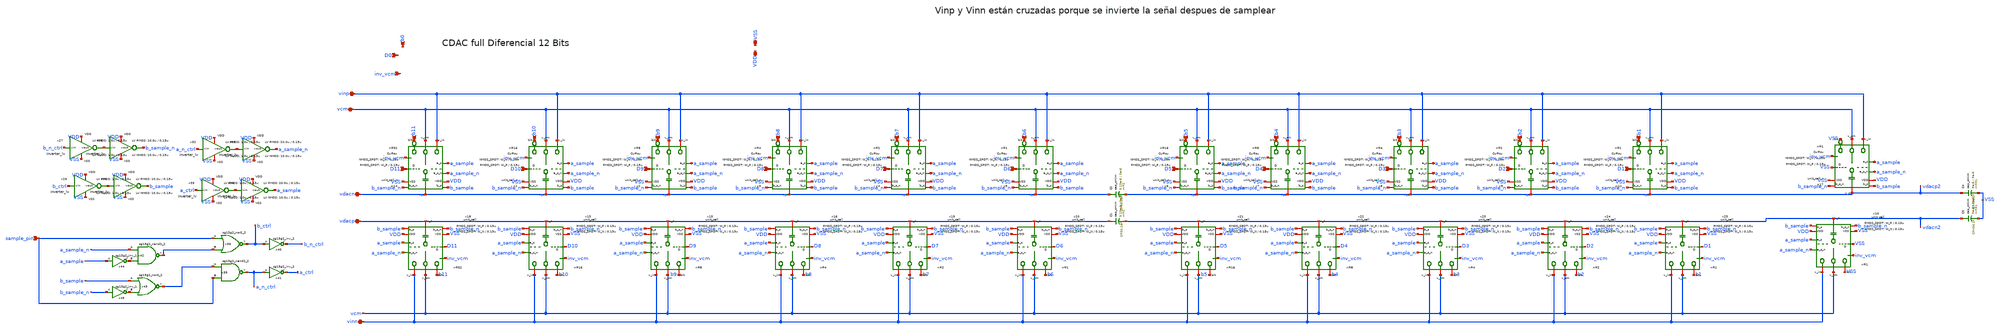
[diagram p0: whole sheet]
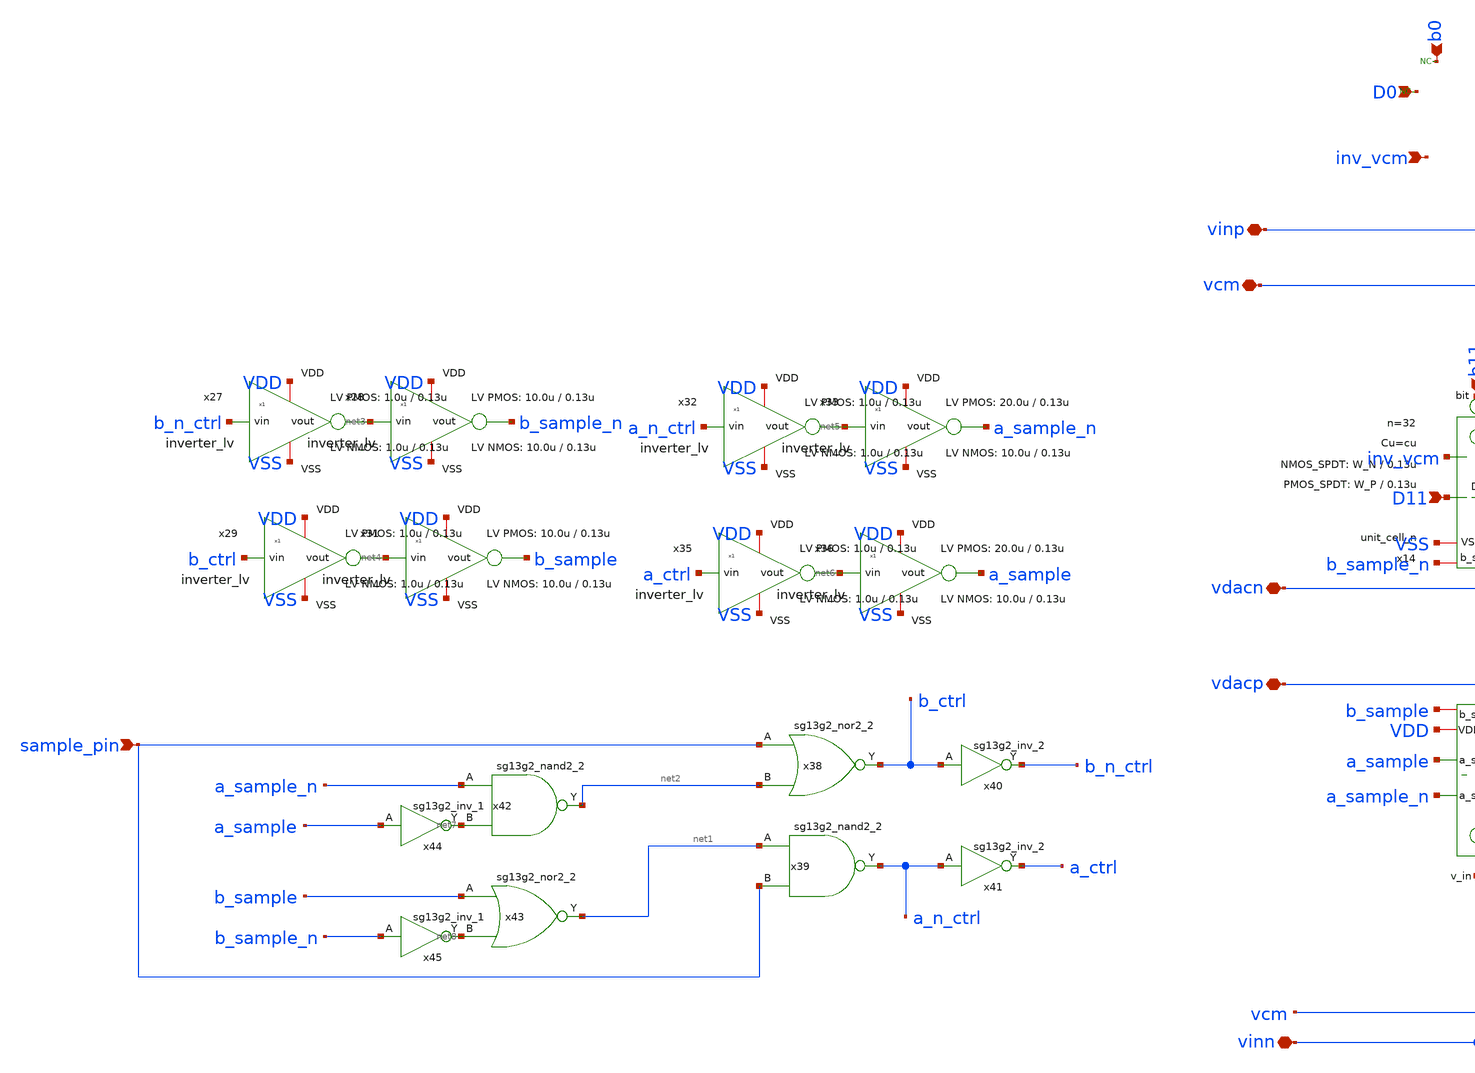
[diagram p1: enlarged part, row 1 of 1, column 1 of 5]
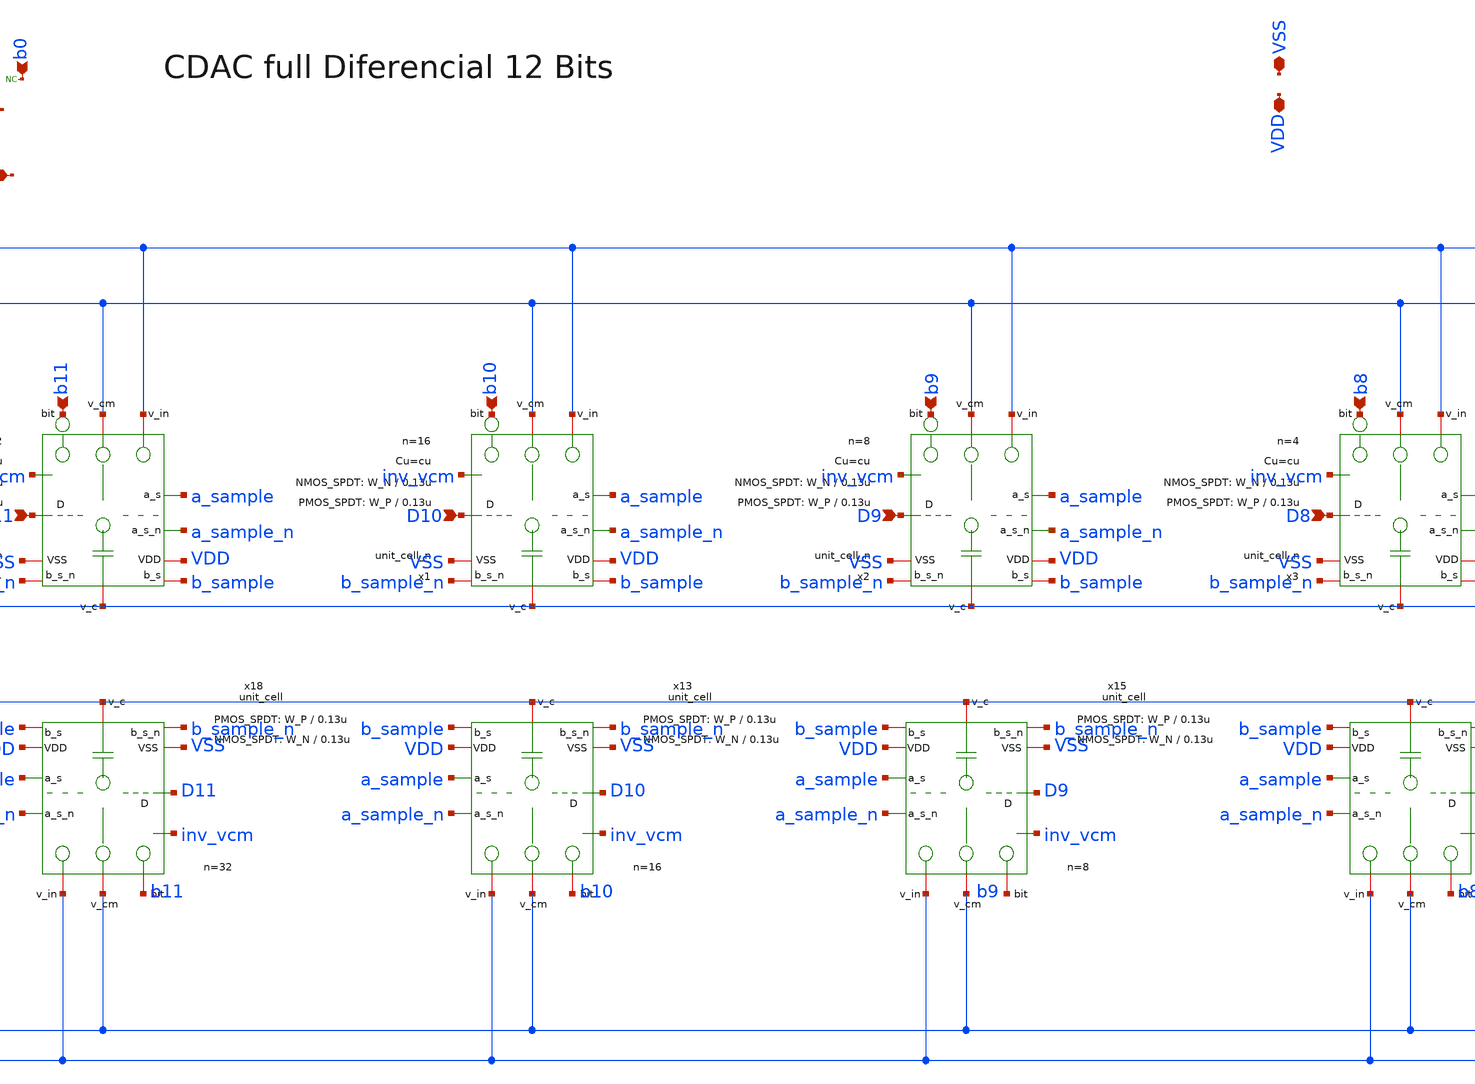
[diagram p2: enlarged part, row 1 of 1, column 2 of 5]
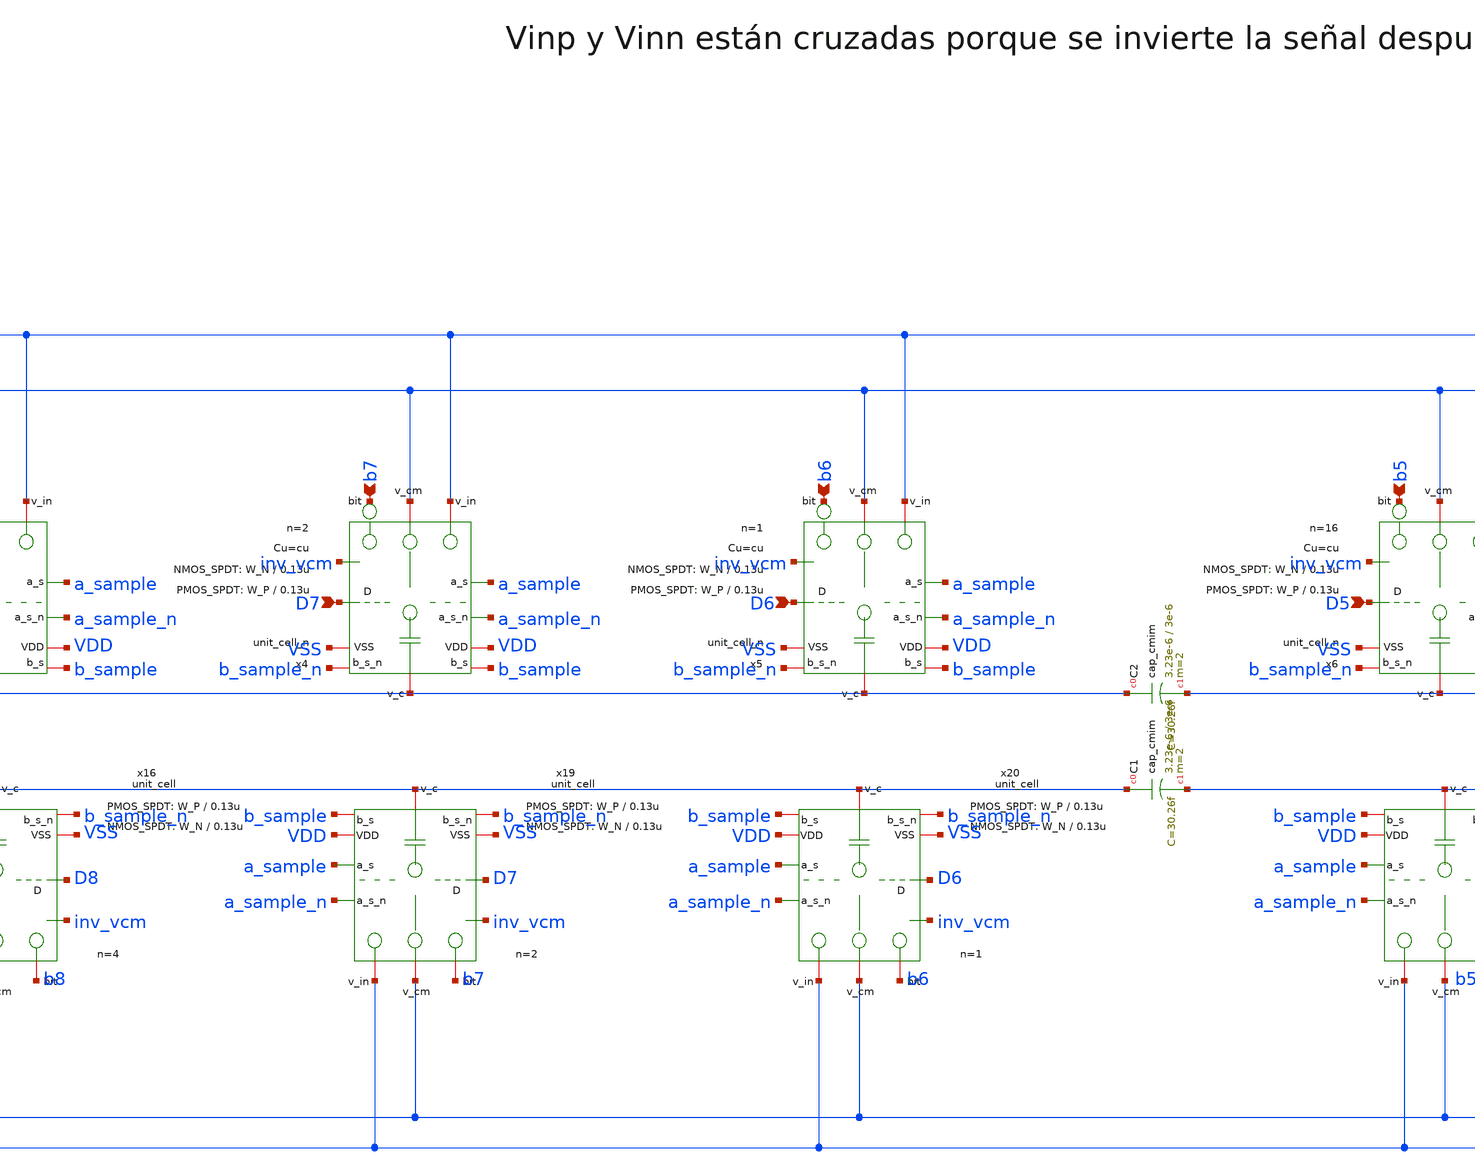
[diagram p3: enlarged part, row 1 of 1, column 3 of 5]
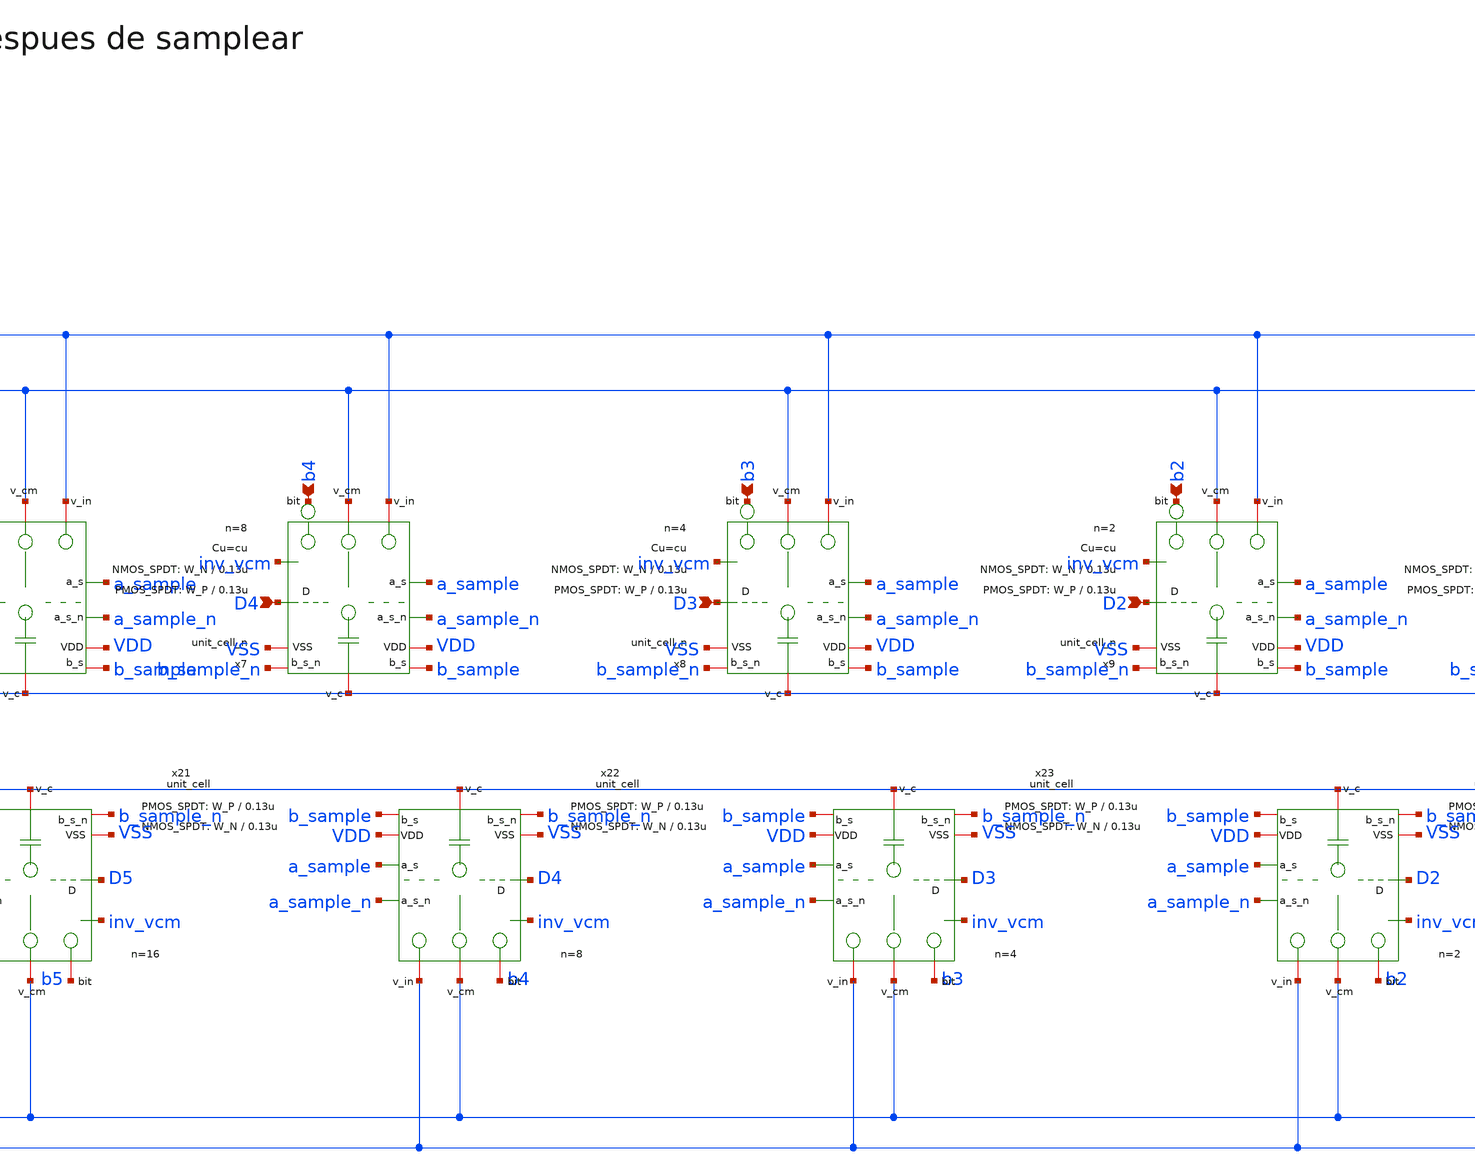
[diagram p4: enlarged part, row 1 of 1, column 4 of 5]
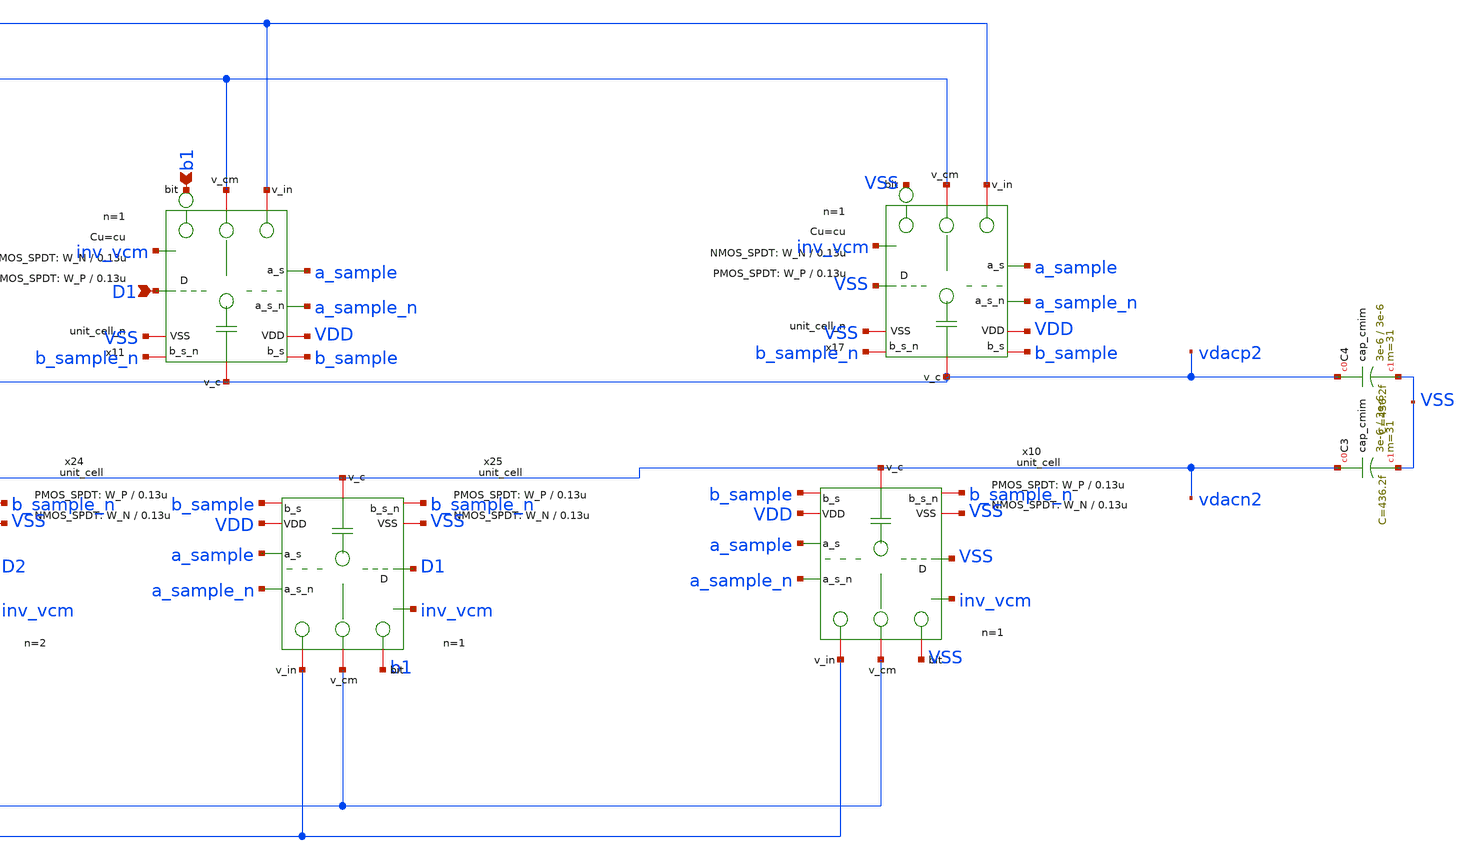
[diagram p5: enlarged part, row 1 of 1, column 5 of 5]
** sch_path: xschem/dac_icms_cell/dac.sch
* IHP-GmbH/IHP-Open-PDK/ihp-sg13g2/libs.tech/xschem/sg13g2_stdcells/sg13g2_inv_2.sch:
* Copyright 2023 IHP PDK Authors
* Licensed under the Apache License, Version 2.0 (the "License");
**.subckt dac D0 b0 vinn vcm sample_pin vinp vdacp vdacn VSS VDD D1 b1 D2 b2 D3 b3 D4 b4 D5 b5 b6 D7
*+ b7 D8 b8 D9 b9 D10 b10 D11 b11 D6 inv_vcm
*.ipin D0
*.ipin b0
*.iopin vinn
*.iopin vcm
*.ipin sample_pin
*.iopin vinp
*.iopin vdacp
*.iopin vdacn
*.iopin VSS
*.iopin VDD
*.ipin D1
*.ipin b1
*.ipin D2
*.ipin b2
*.ipin D3
*.ipin b3
*.ipin D4
*.ipin b4
*.ipin D5
*.ipin b5
*.ipin b6
*.ipin D7
*.ipin b7
*.ipin D8
*.ipin b8
*.ipin D9
*.ipin b9
*.ipin D10
*.ipin b10
*.ipin D11
*.ipin b11
*.ipin D6
*.ipin inv_vcm
x14 VDD D11 VSS vdacn b11 vcm vinp a_sample a_sample_n b_sample b_sample_n inv_vcm unit_cell_n
+ W_P_SPDT=W_P L_P_SPDT=0.13u W_N_SPDT=W_N L_N_SPDT=0.13u Cu=cu n=32
x18 VDD D11 VSS vdacp b11 vcm vinn a_sample a_sample_n b_sample b_sample_n inv_vcm unit_cell
+ W_P_SPDT=W_P L_P_SPDT=0.13u W_N_SPDT=W_N L_N_SPDT=0.13u Cu=cu n=32
x1 VDD D10 VSS vdacn b10 vcm vinp a_sample a_sample_n b_sample b_sample_n inv_vcm unit_cell_n
+ W_P_SPDT=W_P L_P_SPDT=0.13u W_N_SPDT=W_N L_N_SPDT=0.13u Cu=cu n=16
x2 VDD D9 VSS vdacn b9 vcm vinp a_sample a_sample_n b_sample b_sample_n inv_vcm unit_cell_n
+ W_P_SPDT=W_P L_P_SPDT=0.13u W_N_SPDT=W_N L_N_SPDT=0.13u Cu=cu n=8
x3 VDD D8 VSS vdacn b8 vcm vinp a_sample a_sample_n b_sample b_sample_n inv_vcm unit_cell_n
+ W_P_SPDT=W_P L_P_SPDT=0.13u W_N_SPDT=W_N L_N_SPDT=0.13u Cu=cu n=4
x4 VDD D7 VSS vdacn b7 vcm vinp a_sample a_sample_n b_sample b_sample_n inv_vcm unit_cell_n
+ W_P_SPDT=W_P L_P_SPDT=0.13u W_N_SPDT=W_N L_N_SPDT=0.13u Cu=cu n=2
x5 VDD D6 VSS vdacn b6 vcm vinp a_sample a_sample_n b_sample b_sample_n inv_vcm unit_cell_n
+ W_P_SPDT=W_P L_P_SPDT=0.13u W_N_SPDT=W_N L_N_SPDT=0.13u Cu=cu n=1
x6 VDD D5 VSS vdacp2 b5 vcm vinp a_sample a_sample_n b_sample b_sample_n inv_vcm unit_cell_n
+ W_P_SPDT=W_P L_P_SPDT=0.13u W_N_SPDT=W_N L_N_SPDT=0.13u Cu=cu n=16
x7 VDD D4 VSS vdacp2 b4 vcm vinp a_sample a_sample_n b_sample b_sample_n inv_vcm unit_cell_n
+ W_P_SPDT=W_P L_P_SPDT=0.13u W_N_SPDT=W_N L_N_SPDT=0.13u Cu=cu n=8
x8 VDD D3 VSS vdacp2 b3 vcm vinp a_sample a_sample_n b_sample b_sample_n inv_vcm unit_cell_n
+ W_P_SPDT=W_P L_P_SPDT=0.13u W_N_SPDT=W_N L_N_SPDT=0.13u Cu=cu n=4
x9 VDD D2 VSS vdacp2 b2 vcm vinp a_sample a_sample_n b_sample b_sample_n inv_vcm unit_cell_n
+ W_P_SPDT=W_P L_P_SPDT=0.13u W_N_SPDT=W_N L_N_SPDT=0.13u Cu=cu n=2
x11 VDD D1 VSS vdacp2 b1 vcm vinp a_sample a_sample_n b_sample b_sample_n inv_vcm unit_cell_n
+ W_P_SPDT=W_P L_P_SPDT=0.13u W_N_SPDT=W_N L_N_SPDT=0.13u Cu=cu n=1
x13 VDD D10 VSS vdacp b10 vcm vinn a_sample a_sample_n b_sample b_sample_n inv_vcm unit_cell
+ W_P_SPDT=W_P L_P_SPDT=0.13u W_N_SPDT=W_N L_N_SPDT=0.13u Cu=cu n=16
x15 VDD D9 VSS vdacp b9 vcm vinn a_sample a_sample_n b_sample b_sample_n inv_vcm unit_cell
+ W_P_SPDT=W_P L_P_SPDT=0.13u W_N_SPDT=W_N L_N_SPDT=0.13u Cu=cu n=8
x16 VDD D8 VSS vdacp b8 vcm vinn a_sample a_sample_n b_sample b_sample_n inv_vcm unit_cell
+ W_P_SPDT=W_P L_P_SPDT=0.13u W_N_SPDT=W_N L_N_SPDT=0.13u Cu=cu n=4
x19 VDD D7 VSS vdacp b7 vcm vinn a_sample a_sample_n b_sample b_sample_n inv_vcm unit_cell
+ W_P_SPDT=W_P L_P_SPDT=0.13u W_N_SPDT=W_N L_N_SPDT=0.13u Cu=cu n=2
x20 VDD D6 VSS vdacp b6 vcm vinn a_sample a_sample_n b_sample b_sample_n inv_vcm unit_cell
+ W_P_SPDT=W_P L_P_SPDT=0.13u W_N_SPDT=W_N L_N_SPDT=0.13u Cu=cu n=1
x21 VDD D5 VSS vdacn2 b5 vcm vinn a_sample a_sample_n b_sample b_sample_n inv_vcm unit_cell
+ W_P_SPDT=W_P L_P_SPDT=0.13u W_N_SPDT=W_N L_N_SPDT=0.13u Cu=cu n=16
x22 VDD D4 VSS vdacn2 b4 vcm vinn a_sample a_sample_n b_sample b_sample_n inv_vcm unit_cell
+ W_P_SPDT=W_P L_P_SPDT=0.13u W_N_SPDT=W_N L_N_SPDT=0.13u Cu=cu n=8
x23 VDD D3 VSS vdacn2 b3 vcm vinn a_sample a_sample_n b_sample b_sample_n inv_vcm unit_cell
+ W_P_SPDT=W_P L_P_SPDT=0.13u W_N_SPDT=W_N L_N_SPDT=0.13u Cu=cu n=4
x24 VDD D2 VSS vdacn2 b2 vcm vinn a_sample a_sample_n b_sample b_sample_n inv_vcm unit_cell
+ W_P_SPDT=W_P L_P_SPDT=0.13u W_N_SPDT=W_N L_N_SPDT=0.13u Cu=cu n=2
x25 VDD D1 VSS vdacn2 b1 vcm vinn a_sample a_sample_n b_sample b_sample_n inv_vcm unit_cell
+ W_P_SPDT=W_P L_P_SPDT=0.13u W_N_SPDT=W_N L_N_SPDT=0.13u Cu=cu n=1
x27 VDD b_n_ctrl net3 VSS inverter_lv W_P=1.0u L_P=0.13u W_N=1.0u L_N=0.13u N_C=1
x28 VDD net3 b_sample_n VSS inverter_lv W_P=10.0u L_P=0.13u W_N=10.0u L_N=0.13u N_C=1
x29 VDD b_ctrl net4 VSS inverter_lv W_P=1.0u L_P=0.13u W_N=1.0u L_N=0.13u N_C=1
x31 VDD net4 b_sample VSS inverter_lv W_P=10.0u L_P=0.13u W_N=10.0u L_N=0.13u N_C=1
x32 VDD a_n_ctrl net5 VSS inverter_lv W_P=1.0u L_P=0.13u W_N=1.0u L_N=0.13u N_C=1
x33 VDD net5 a_sample_n VSS inverter_lv W_P=20.0u L_P=0.13u W_N=10.0u L_N=0.13u N_C=1
x35 VDD a_ctrl net6 VSS inverter_lv W_P=1.0u L_P=0.13u W_N=1.0u L_N=0.13u N_C=1
x36 VDD net6 a_sample VSS inverter_lv W_P=20.0u L_P=0.13u W_N=10.0u L_N=0.13u N_C=1
x38 b_ctrl sample_pin net2 VDD VSS sg13g2_nor2_2
x39 a_n_ctrl net1 sample_pin VDD VSS sg13g2_nand2_2
x40 b_n_ctrl b_ctrl VDD VSS sg13g2_inv_2
x41 a_ctrl a_n_ctrl VDD VSS sg13g2_inv_2
x42 net2 a_sample_n net7 VDD VSS sg13g2_nand2_2
x43 net1 b_sample net8 VDD VSS sg13g2_nor2_2
x44 net7 a_sample VDD VSS sg13g2_inv_1
x45 net8 b_sample_n VDD VSS sg13g2_inv_1
XC1 vdacp vdacn2 cap_cmim w=3.23e-6 l=3e-6 m=2 mm_ok=1
XC2 vdacn vdacp2 cap_cmim w=3.23e-6 l=3e-6 m=2 mm_ok=1
x10 VDD VSS VSS vdacn2 VSS vcm vinn a_sample a_sample_n b_sample b_sample_n inv_vcm unit_cell
+ W_P_SPDT=W_P L_P_SPDT=0.13u W_N_SPDT=W_N L_N_SPDT=0.13u Cu=cu n=1
x17 VDD VSS VSS vdacp2 VSS vcm vinp a_sample a_sample_n b_sample b_sample_n inv_vcm unit_cell_n
+ W_P_SPDT=W_P L_P_SPDT=0.13u W_N_SPDT=W_N L_N_SPDT=0.13u Cu=cu n=1
XC3 vdacn2 VSS cap_cmim w=3e-6 l=3e-6 m=31 mm_ok=1
XC4 vdacp2 VSS cap_cmim w=3e-6 l=3e-6 m=31 mm_ok=1
* noconn b0
* noconn D0
**.ends

* expanding   symbol:  dac_icms_cell/unit_cell_n.sym # of pins=12
** sym_path: xschem/dac_icms_cell/unit_cell_n.sym
** sch_path: xschem/dac_icms_cell/unit_cell_n.sch
.subckt unit_cell_n VDD d VSS v_top bit v_cm v_in a_sample a_sample_n b_sample b_sample_n inv_vcm
+  W_P_SPDT=1.0u L_P_SPDT=0.13u W_N_SPDT=1.0u L_N_SPDT=0.13u Cu=8f n=1
*.iopin v_top
*.ipin a_sample
*.ipin a_sample_n
*.ipin b_sample
*.ipin b_sample_n
*.iopin v_in
*.ipin d
*.iopin v_cm
*.ipin bit
*.ipin inv_vcm
*.iopin VSS
*.iopin VDD
x2 VDD a_sample VSS v_top v_cm a_sample_n transmission_gate_lv_wo_dummy W_P=W_P_SPDT L_P=L_P_SPDT
+ W_N=W_N_SPDT L_N=L_N_SPDT W_P_D=1.0u L_P_D=0.13u W_N_D=1.0u L_N_D=0.13u n=n
XC1 TOP_C v_top cap_cmim w=3e-6 l=3e-6 m=n mm_ok=1
XM1 TOP_C net3 VSS VSS sg13_lv_nmos w=4u l=0.13u ng=1 m=n mm_ok=1
XM3 TOP_C net4 VDD VDD sg13_lv_pmos w=4u l=0.13u ng=1 m=n mm_ok=1
x3 VDD net2 VSS TOP_C v_cm net1 transmission_gate_lv_wo_dummy W_P=W_P_SPDT L_P=L_P_SPDT W_N=W_N_SPDT
+ L_N=L_N_SPDT W_P_D=1.0u L_P_D=0.13u W_N_D=1.0u L_N_D=0.13u n=n
x4 VDD b_sample_n VSS TOP_C v_in b_sample transmission_gate_lv_w_dummy W_P=W_P_SPDT L_P=L_P_SPDT
+ W_N=W_N_SPDT L_N=L_N_SPDT W_P_D=1.0u L_P_D=0.13u W_N_D=1.0u L_N_D=0.13u n=n
x23 net5 bit d VDD VSS sg13g2_nand2_1
x46 net6 net8 d VDD VSS sg13g2_and2_1
x5 VDD net5 net4 VSS buffer_lv W_P_INV=3.0u L_P_INV=0.13u W_N_INV=1.0u L_N_INV=0.13u
x6 VDD net6 net3 VSS buffer_lv W_P_INV=3.0u L_P_INV=0.13u W_N_INV=1.0u L_N_INV=0.13u
x7 VDD net9 net2 VSS buffer_lv W_P_INV=3.0u L_P_INV=0.13u W_N_INV=1.0u L_N_INV=0.13u
x9 VDD net7 net1 VSS buffer_lv W_P_INV=3.0u L_P_INV=0.13u W_N_INV=1.0u L_N_INV=0.13u
x32 net8 bit VDD VSS sg13g2_inv_1
x1 net9 d sample VDD VSS sg13g2_nor2_1
x8 net10 d sample VDD VSS sg13g2_or2_1
.ends


* expanding   symbol:  dac_icms_cell/unit_cell.sym # of pins=12
** sym_path: xschem/dac_icms_cell/unit_cell.sym
** sch_path: xschem/dac_icms_cell/unit_cell.sch
.subckt unit_cell VDD d VSS v_top bit v_cm v_in a_sample a_sample_n b_sample b_sample_n inv_vcm
+  W_P_SPDT=1.0u L_P_SPDT=0.13u W_N_SPDT=1.0u L_N_SPDT=0.13u Cu=8f n=1
*.iopin v_top
*.ipin a_sample
*.ipin a_sample_n
*.ipin b_sample
*.ipin b_sample_n
*.iopin v_in
*.ipin d
*.iopin v_cm
*.ipin bit
*.ipin inv_vcm
*.iopin VSS
*.iopin VDD
x2 VDD a_sample VSS v_top v_cm a_sample_n transmission_gate_lv_wo_dummy W_P=W_P_SPDT L_P=L_P_SPDT
+ W_N=W_N_SPDT L_N=L_N_SPDT W_P_D=1.0u L_P_D=0.13u W_N_D=1.0u L_N_D=0.13u n=n
XC1 net1 v_top cap_cmim w=3e-6 l=3e-6 m=n mm_ok=1
XM1 net1 net4 VSS VSS sg13_lv_nmos w=4u l=0.13u ng=1 m=n mm_ok=1
XM3 net1 net5 VDD VDD sg13_lv_pmos w=4u l=0.13u ng=1 m=n mm_ok=1
x3 VDD net3 VSS net1 v_cm net2 transmission_gate_lv_wo_dummy W_P=W_P_SPDT L_P=L_P_SPDT W_N=W_N_SPDT
+ L_N=L_N_SPDT W_P_D=1.0u L_P_D=0.13u W_N_D=1.0u L_N_D=0.13u n=n
x4 VDD b_sample_n VSS net1 v_in b_sample transmission_gate_lv_w_dummy W_P=W_P_SPDT L_P=L_P_SPDT
+ W_N=W_N_SPDT L_N=L_N_SPDT W_P_D=1.0u L_P_D=0.13u W_N_D=1.0u L_N_D=0.13u n=n
x23 net6 net10 d VDD VSS sg13g2_nand2_1
x46 net7 bit d VDD VSS sg13g2_and2_1
x5 VDD net6 net5 VSS buffer_lv W_P_INV=3.0u L_P_INV=0.13u W_N_INV=1.0u L_N_INV=0.13u
x6 VDD net7 net4 VSS buffer_lv W_P_INV=3.0u L_P_INV=0.13u W_N_INV=1.0u L_N_INV=0.13u
x7 VDD net9 net3 VSS buffer_lv W_P_INV=3.0u L_P_INV=0.13u W_N_INV=1.0u L_N_INV=0.13u
x9 VDD net8 net2 VSS buffer_lv W_P_INV=3.0u L_P_INV=0.13u W_N_INV=1.0u L_N_INV=0.13u
x32 net10 bit VDD VSS sg13g2_inv_1
x10 net9 net11 inv_vcm VDD VSS sg13g2_and2_1
x11 net11 b_sample VDD VSS sg13g2_inv_1
x12 net8 net9 VDD VSS sg13g2_inv_1
.ends


* expanding   symbol:  inverter/inverter_lv.sym # of pins=4
** sym_path: xschem/inverter/inverter_lv.sym
** sch_path: xschem/inverter/inverter_lv.sch
.subckt inverter_lv VDD vin vout VSS  W_P=3.0u L_P=0.13u W_N=1.0u L_N=0.13u N_C=1
*.ipin vin
*.iopin VDD
*.iopin VSS
*.opin vout
XM1 vout vin VDD VDD sg13_lv_pmos w=W_P l=L_P ng=1 m={N_C} mm_ok=1
XM2 vout vin VSS VSS sg13_lv_nmos w=W_N l=L_N ng=1 m={N_C} mm_ok=1
.ends


* expanding   symbol:  sg13g2_stdcells/sg13g2_nor2_2.sym # of pins=3
** sym_path: sg13g2_stdcells/sg13g2_nor2_2.sym
** sch_path: sg13g2_stdcells/sg13g2_nor2_2.sch
.subckt sg13g2_nor2_2 Y A B VDD VSS
*.opin Y
*.ipin B
*.ipin A
*.iopin VDD
*.iopin VSS
XM1 Y A VSS VSS sg13_lv_nmos w=1.48u l=130.00n ng=2 m=1 mm_ok=1
XM2 Y B VSS VSS sg13_lv_nmos w=1.48u l=130.00n ng=2 m=1 mm_ok=1
XM3 net1 A VDD VDD sg13_lv_pmos w=2.24u l=130.00n ng=2 m=1 mm_ok=1
XM4 Y B net1 VDD sg13_lv_pmos w=2.24u l=130.00n ng=2 m=1 mm_ok=1
.ends


* expanding   symbol:  sg13g2_stdcells/sg13g2_nand2_2.sym # of pins=3
** sym_path: sg13g2_stdcells/sg13g2_nand2_2.sym
** sch_path: sg13g2_stdcells/sg13g2_nand2_2.sch
.subckt sg13g2_nand2_2 Y A B VDD VSS
*.iopin VDD
*.iopin VSS
*.opin Y
*.ipin B
*.ipin A
XM1 Y A net1 VSS sg13_lv_nmos w=1.44u l=130.00n ng=2 m=1 mm_ok=1
XM2 net1 B VSS VSS sg13_lv_nmos w=1.44u l=130.00n ng=2 m=1 mm_ok=1
XM3 Y A VDD VDD sg13_lv_pmos w=2.24u l=130.00n ng=2 m=1 mm_ok=1
XM4 Y B VDD VDD sg13_lv_pmos w=2.24u l=130.00n ng=2 m=1 mm_ok=1
.ends


* expanding   symbol:  sg13g2_stdcells/sg13g2_inv_2.sym # of pins=2
** sym_path: sg13g2_stdcells/sg13g2_inv_2.sym
** sch_path: sg13g2_stdcells/sg13g2_inv_2.sch
.subckt sg13g2_inv_2 Y A VDD VSS
*.opin Y
*.ipin A
*.iopin VDD
*.iopin VSS
XM1 Y A VSS VSS sg13_lv_nmos w=1.48u l=130.00n ng=2 m=1 mm_ok=1
XM2 Y A VDD VDD sg13_lv_pmos w=2.24u l=130.00n ng=2 m=1 mm_ok=1
.ends


* expanding   symbol:  sg13g2_stdcells/sg13g2_inv_1.sym # of pins=2
** sym_path: sg13g2_stdcells/sg13g2_inv_1.sym
** sch_path: sg13g2_stdcells/sg13g2_inv_1.sch
.subckt sg13g2_inv_1 Y A VDD VSS
*.opin Y
*.ipin A
*.iopin VDD
*.iopin VSS
XM1 Y A VSS VSS sg13_lv_nmos w=740.00n l=130.00n ng=1 m=1 mm_ok=1
XM2 Y A VDD VDD sg13_lv_pmos w=1.12u l=130.00n ng=1 m=1 mm_ok=1
.ends


* expanding   symbol:  transmission_gate/transmission_gate_lv_wo_dummy.sym # of pins=6
** sym_path: xschem/transmission_gate/transmission_gate_lv_wo_dummy.sym
** sch_path: xschem/transmission_gate/transmission_gate_lv_wo_dummy.sch
.subckt transmission_gate_lv_wo_dummy VDD di_tg_ctrl VSS v_b v_a di_tg_ctrl_n  W_P=2.0u L_P=0.13u
+ W_N=2.0u L_N=0.13u W_P_D=1.0u L_P_D=0.13u W_N_D=1.0u L_N_D=0.13u n=1
*.iopin v_a
*.iopin v_b
*.iopin VDD
*.iopin VSS
*.ipin di_tg_ctrl
*.ipin di_tg_ctrl_n
XM1 v_a di_tg_ctrl v_b VSS sg13_lv_nmos w=W_N l=L_N ng=1 m=n mm_ok=1
XM2 v_a di_tg_ctrl_n v_b VDD sg13_lv_pmos w=W_P l=L_P ng=1 m=n mm_ok=1
.ends


* expanding   symbol:  transmission_gate/transmission_gate_lv_w_dummy.sym # of pins=6
** sym_path: xschem/transmission_gate/transmission_gate_lv_w_dummy.sym
** sch_path: xschem/transmission_gate/transmission_gate_lv_w_dummy.sch
.subckt transmission_gate_lv_w_dummy VDD di_tg_ctrl VSS v_b v_a di_tg_ctrl_n  W_P=2.0u L_P=0.13u
+ W_N=2.0u L_N=0.13u W_P_D=1.0u L_P_D=0.13u W_N_D=1.0u L_N_D=0.13u n=1
*.iopin v_a
*.iopin v_b
*.iopin VDD
*.iopin VSS
*.ipin di_tg_ctrl
*.ipin di_tg_ctrl_n
XM1 v_a di_tg_ctrl v_b VSS sg13_lv_nmos w=W_N l=L_N ng=1 m=n mm_ok=1
XM2 v_a di_tg_ctrl_n v_b VDD sg13_lv_pmos w=W_P l=L_P ng=1 m=n mm_ok=1
XMdummy2 v_b di_tg_ctrl v_b VDD sg13_lv_pmos w=W_P l=L_P ng=1 m={n/2} mm_ok=1
XMdummy1 v_b di_tg_ctrl_n v_b VSS sg13_lv_nmos w=W_N l=L_N ng=1 m={n/2} mm_ok=1
.ends


* expanding   symbol:  sg13g2_stdcells/sg13g2_nand2_1.sym # of pins=3
** sym_path: sg13g2_stdcells/sg13g2_nand2_1.sym
** sch_path: sg13g2_stdcells/sg13g2_nand2_1.sch
.subckt sg13g2_nand2_1 Y A B VDD VSS
*.iopin VDD
*.iopin VSS
*.ipin A
*.ipin B
*.opin Y
XM1 Y A net1 VSS sg13_lv_nmos w=740.00n l=130.00n ng=1 m=1 mm_ok=1
XM2 net1 B VSS VSS sg13_lv_nmos w=740.00n l=130.00n ng=1 m=1 mm_ok=1
XM3 Y A VDD VDD sg13_lv_pmos w=1.12u l=130.00n ng=1 m=1 mm_ok=1
XM4 Y B VDD VDD sg13_lv_pmos w=1.12u l=130.00n ng=1 m=1 mm_ok=1
.ends


* expanding   symbol:  sg13g2_stdcells/sg13g2_and2_1.sym # of pins=3
** sym_path: sg13g2_stdcells/sg13g2_and2_1.sym
** sch_path: sg13g2_stdcells/sg13g2_and2_1.sch
.subckt sg13g2_and2_1 X A B VDD VSS
*.ipin A
*.ipin B
*.opin X
*.iopin VDD
*.iopin VSS
XM1 net1 A net2 VSS sg13_lv_nmos w=640.00n l=130.00n ng=1 m=1 mm_ok=1
XM2 net2 B VSS VSS sg13_lv_nmos w=640.00n l=130.00n ng=1 m=1 mm_ok=1
XM3 X net1 VSS VSS sg13_lv_nmos w=740.00n l=130.00n ng=1 m=1 mm_ok=1
XM4 net1 B VDD VDD sg13_lv_pmos w=840.00n l=130.00n ng=1 m=1 mm_ok=1
XM5 net1 A VDD VDD sg13_lv_pmos w=840.00n l=130.00n ng=1 m=1 mm_ok=1
XM6 X net1 VDD VDD sg13_lv_pmos w=1.12u l=130.00n ng=1 m=1 mm_ok=1
.ends


* expanding   symbol:  buffer/buffer_lv.sym # of pins=4
** sym_path: buffer/buffer_lv.sym
** sch_path: buffer/buffer_lv.sch
.subckt buffer_lv VDD vin vout VSS  W_P_INV=3.0u L_P_INV=0.13u W_N_INV=1.0u L_N_INV=0.13u
*.ipin vin
*.iopin VDD
*.iopin VSS
*.opin vout
x1 VDD vin net1 VSS inverter_lv W_P=W_P_INV L_P=L_P_INV W_N=W_N_INV L_N=L_N_INV N_C=1
x2 VDD net1 vout VSS inverter_lv W_P=W_P_INV L_P=L_P_INV W_N=W_N_INV L_N=L_N_INV N_C=1
.ends


* expanding   symbol:  sg13g2_stdcells/sg13g2_nor2_1.sym # of pins=3
** sym_path: sg13g2_stdcells/sg13g2_nor2_1.sym
** sch_path: sg13g2_stdcells/sg13g2_nor2_1.sch
.subckt sg13g2_nor2_1 Y A B VDD VSS
*.opin Y
*.ipin B
*.ipin A
*.iopin VDD
*.iopin VSS
XM1 Y A VSS VSS sg13_lv_nmos w=740.00n l=130.00n ng=1 m=1 mm_ok=1
XM2 Y B VSS VSS sg13_lv_nmos w=740.00n l=130.00n ng=1 m=1 mm_ok=1
XM3 net1 A VDD VDD sg13_lv_pmos w=1.12u l=130.00n ng=1 m=1 mm_ok=1
XM4 Y B net1 VDD sg13_lv_pmos w=1.12u l=130.00n ng=1 m=1 mm_ok=1
.ends


* expanding   symbol:  sg13g2_stdcells/sg13g2_or2_1.sym # of pins=3
** sym_path: sg13g2_stdcells/sg13g2_or2_1.sym
** sch_path: sg13g2_stdcells/sg13g2_or2_1.sch
.subckt sg13g2_or2_1 X A B VDD VSS
*.opin X
*.ipin B
*.ipin A
*.iopin VDD
*.iopin VSS
XM1 net1 B VSS VSS sg13_lv_nmos w=550.00n l=130.00n ng=1 m=1 mm_ok=1
XM2 net1 A VSS VSS sg13_lv_nmos w=550.00n l=130.00n ng=1 m=1 mm_ok=1
XM3 X net1 VSS VSS sg13_lv_nmos w=740.00n l=130.00n ng=1 m=1 mm_ok=1
XM4 net2 A VDD VDD sg13_lv_pmos w=840.00n l=130.00n ng=1 m=1 mm_ok=1
XM5 net1 B net2 VDD sg13_lv_pmos w=840.00n l=130.00n ng=1 m=1 mm_ok=1
XM6 X net1 VDD VDD sg13_lv_pmos w=1.12u l=130.00n ng=1 m=1 mm_ok=1
.ends

.end
